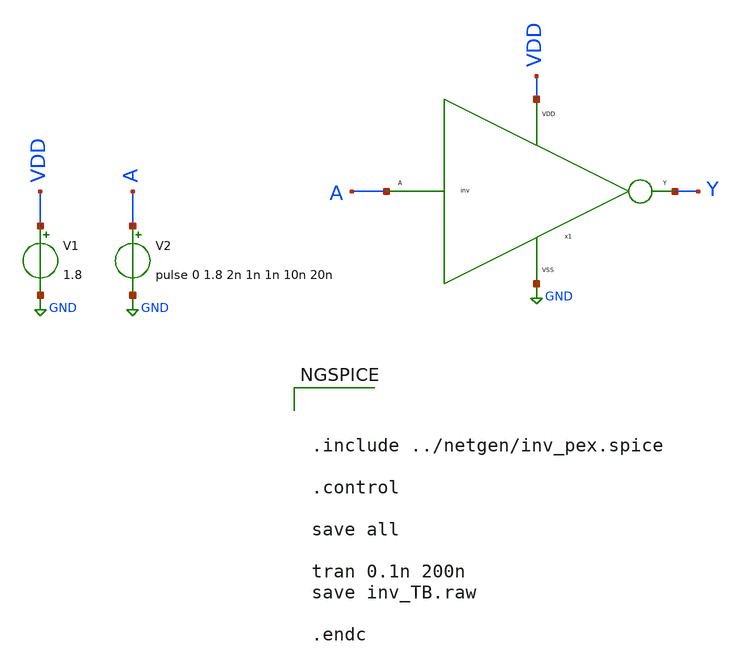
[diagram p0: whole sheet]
** sch_path: takim_adi_FINAL/xschem/inv_TB.sch
**.subckt inv_TB
x1 A Y VDD GND inv
V1 VDD GND 1.8
V2 A GND pulse 0 1.8 2n 1n 1n 10n 20n
**** begin user architecture code

** opencircuitdesign pdks install
.lib $::SKYWATER_MODELS/sky130.lib.spice tt_mm





.include ../netgen/inv_pex.spice

.control

save all

tran 0.1n 200n
save inv_TB.raw

.endc


**** end user architecture code
**.ends
.GLOBAL GND
.end
